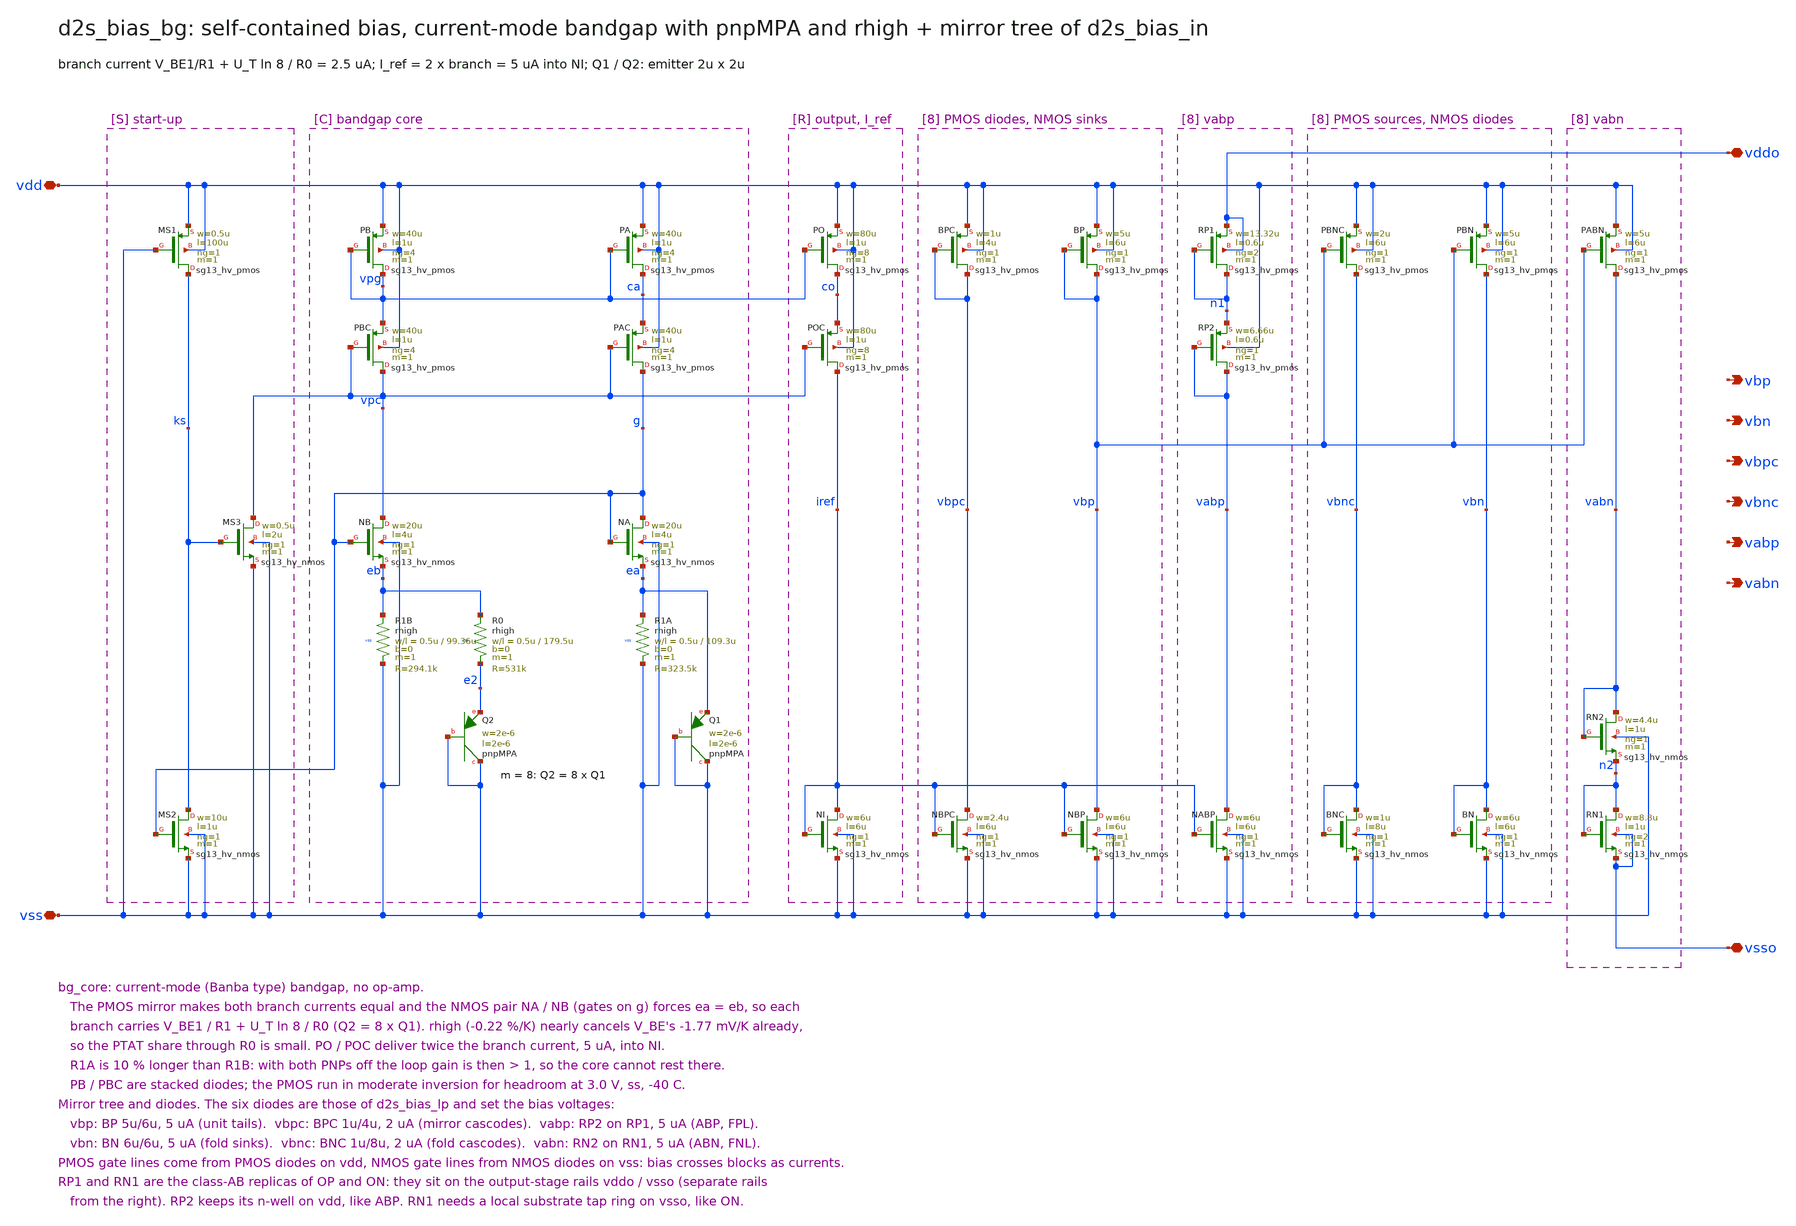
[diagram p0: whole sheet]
** sch_path: sudelbuecher/design_considerations/class_ab_pad_driver/improvements/xschem/d2s_bias_bg.sch
**.subckt d2s_bias_bg vdd vss vddo vsso vbp vbn vbpc vbnc vabp vabn
*.iopin vdd
*.iopin vss
*.iopin vddo
*.iopin vsso
*.opin vbp
*.opin vbn
*.opin vbpc
*.opin vbnc
*.opin vabp
*.opin vabn
XMS1 ks vss vdd vdd sg13_hv_pmos w=0.5u l=100u ng=1 m=1 mm_ok=1
XMS2 ks g vss vss sg13_hv_nmos w=10u l=1u ng=1 m=1 mm_ok=1
XMS3 vpc ks vss vss sg13_hv_nmos w=0.5u l=2u ng=1 m=1 mm_ok=1
XPB vpg vpg vdd vdd sg13_hv_pmos w=40u l=1u ng=4 m=1 mm_ok=1
XPBC vpc vpc vpg vdd sg13_hv_pmos w=40u l=1u ng=4 m=1 mm_ok=1
XNB vpc g eb vss sg13_hv_nmos w=20u l=4u ng=1 m=1 mm_ok=1
XR1B eb vss vss rhigh w=0.5u l=99.36u m=1 b=0 mm_ok=1
XR0 eb e2 vss rhigh w=0.5u l=179.5u m=1 b=0 mm_ok=1
XQ2 vss vss e2 pnpMPA a=4p p=8u m=8
XPA ca vpg vdd vdd sg13_hv_pmos w=40u l=1u ng=4 m=1 mm_ok=1
XPAC g vpc ca vdd sg13_hv_pmos w=40u l=1u ng=4 m=1 mm_ok=1
XNA g g ea vss sg13_hv_nmos w=20u l=4u ng=1 m=1 mm_ok=1
XR1A ea vss vss rhigh w=0.5u l=109.3u m=1 b=0 mm_ok=1
XQ1 vss vss ea pnpMPA a=4p p=8u m=1
XPO co vpg vdd vdd sg13_hv_pmos w=80u l=1u ng=8 m=1 mm_ok=1
XPOC iref vpc co vdd sg13_hv_pmos w=80u l=1u ng=8 m=1 mm_ok=1
XNI iref iref vss vss sg13_hv_nmos w=6u l=6u ng=1 m=1 mm_ok=1
XBPC vbpc vbpc vdd vdd sg13_hv_pmos w=1u l=4u ng=1 m=1 mm_ok=1
XNBPC vbpc iref vss vss sg13_hv_nmos w=2.4u l=6u ng=1 m=1 mm_ok=1
XBP vbp vbp vdd vdd sg13_hv_pmos w=5u l=6u ng=1 m=1 mm_ok=1
XNBP vbp iref vss vss sg13_hv_nmos w=6u l=6u ng=1 m=1 mm_ok=1
XRP1 n1 n1 vddo vddo sg13_hv_pmos w=13.32u l=0.6u ng=2 m=1 mm_ok=1
XRP2 vabp vabp n1 vdd sg13_hv_pmos w=6.66u l=0.6u ng=1 m=1 mm_ok=1
XNABP vabp iref vss vss sg13_hv_nmos w=6u l=6u ng=1 m=1 mm_ok=1
XPBNC vbnc vbp vdd vdd sg13_hv_pmos w=2u l=6u ng=1 m=1 mm_ok=1
XBNC vbnc vbnc vss vss sg13_hv_nmos w=1u l=8u ng=1 m=1 mm_ok=1
XPBN vbn vbp vdd vdd sg13_hv_pmos w=5u l=6u ng=1 m=1 mm_ok=1
XBN vbn vbn vss vss sg13_hv_nmos w=6u l=6u ng=1 m=1 mm_ok=1
XPABN vabn vbp vdd vdd sg13_hv_pmos w=5u l=6u ng=1 m=1 mm_ok=1
XRN2 vabn vabn n2 vss sg13_hv_nmos w=4.4u l=1u ng=1 m=1 mm_ok=1
XRN1 n2 n2 vsso vsso sg13_hv_nmos w=8.8u l=1u ng=2 m=1 mm_ok=1
**.ends
.end
